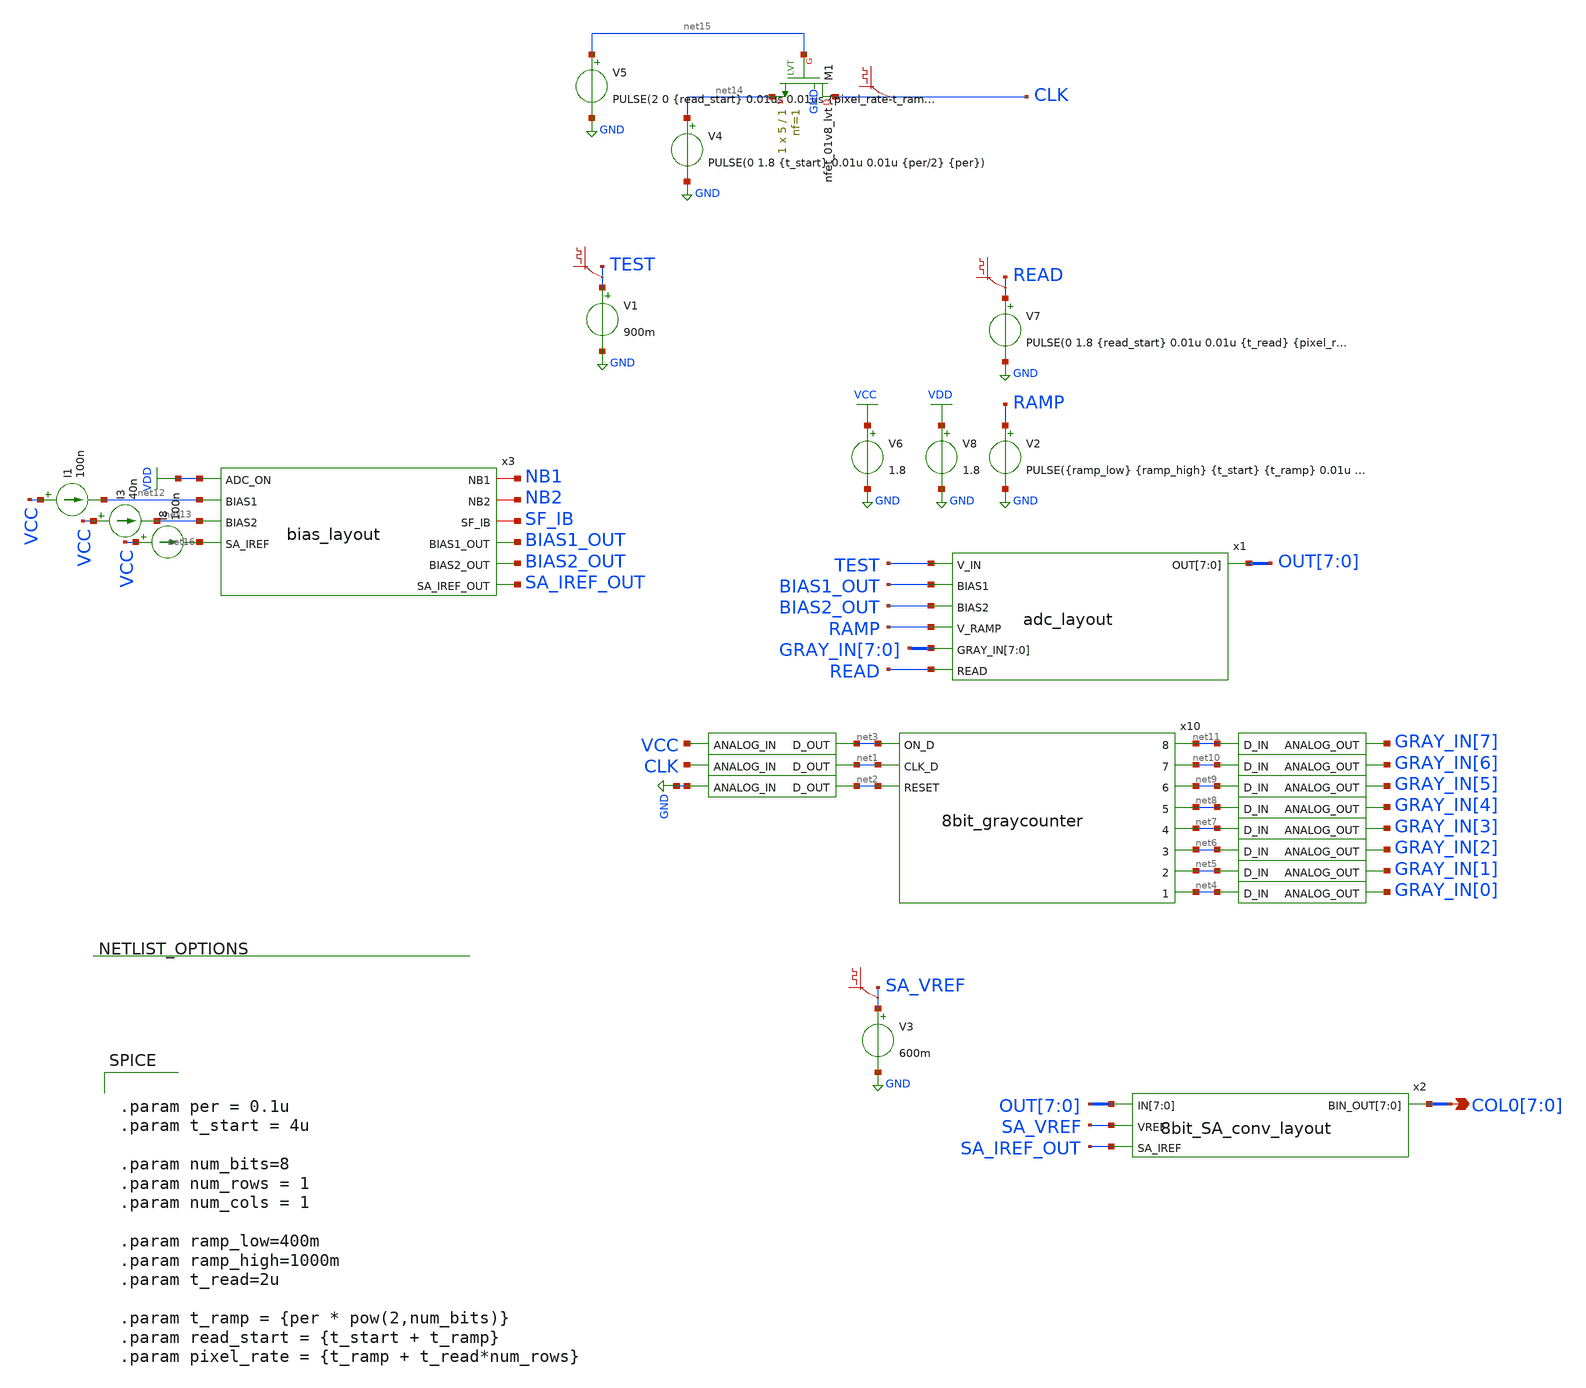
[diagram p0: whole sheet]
** sch_path: xschem/testbench/adc_layout_tb.sch
**.subckt adc_layout_tb COL0[7],COL0[6],COL0[5],COL0[4],COL0[3],COL0[2],COL0[1],COL0[0]
*.opin COL0[7],COL0[6],COL0[5],COL0[4],COL0[3],COL0[2],COL0[1],COL0[0]
V8 VDD GND 1.8
x6 net2 GND adc_bridge
x8 net3 VCC adc_bridge
x7 net1 CLK adc_bridge
x10 net11 net3 net10 net1 net9 net8 net2 net7 net6 net5 net4 8bit_graycounter
x5 GRAY_IN[7] net11 dac_bridge
x9 GRAY_IN[6] net10 dac_bridge
x11 GRAY_IN[5] net9 dac_bridge
x12 GRAY_IN[4] net8 dac_bridge
x13 GRAY_IN[3] net7 dac_bridge
x14 GRAY_IN[2] net6 dac_bridge
x15 GRAY_IN[1] net5 dac_bridge
x16 GRAY_IN[0] net4 dac_bridge
I1 VCC net12 100n
I3 VCC net13 40n
I8 VCC net16 100n
V2 RAMP GND PULSE({ramp_low} {ramp_high} {t_start} {t_ramp} 0.01u {pixel_rate-t_ramp} {pixel_rate})
V7 READ GND PULSE(0 1.8 {read_start} 0.01u 0.01u {t_read} {pixel_rate})
.save v(read)
V1 TEST GND 900m
.save v(test)
V3 SA_VREF GND 600m
.save v(sa_vref)
V4 net14 GND PULSE(0 1.8 {t_start} 0.01u 0.01u {per/2} {per})
V5 net15 GND PULSE(2 0 {read_start} 0.01us 0.01us {pixel_rate-t_ramp} {pixel_rate})
.save v(clk)
XM1 CLK net15 net14 GND sky130_fd_pr__nfet_01v8_lvt L=1 W=5 nf=1 ad='int((nf+1)/2) * W/nf * 0.29' as='int((nf+2)/2) * W/nf * 0.29'
+ pd='2*int((nf+1)/2) * (W/nf + 0.29)' ps='2*int((nf+2)/2) * (W/nf + 0.29)' nrd='0.29 / W' nrs='0.29 / W'
+ sa=0 sb=0 sd=0 mult=1 m=1
V6 VCC GND 1.8
x1 TEST BIAS1_OUT OUT[7] OUT[6] OUT[5] OUT[4] OUT[3] OUT[2] OUT[1] OUT[0] BIAS2_OUT RAMP GRAY_IN[7]
+ GRAY_IN[6] GRAY_IN[5] GRAY_IN[4] GRAY_IN[3] GRAY_IN[2] GRAY_IN[1] GRAY_IN[0] READ adc_layout
x2 OUT[7] OUT[6] OUT[5] OUT[4] OUT[3] OUT[2] OUT[1] OUT[0] SA_VREF SA_IREF_OUT COL0[7] COL0[6]
+ COL0[5] COL0[4] COL0[3] COL0[2] COL0[1] COL0[0] 8bit_SA_conv_layout
x3 NB1 NB2 SF_IB VDD net12 BIAS1_OUT BIAS2_OUT net13 SA_IREF_OUT net16 bias_layout
**** begin user architecture code


.param per = 0.1u
.param t_start = 4u

.param num_bits=8
.param num_rows = 1
.param num_cols = 1

.param ramp_low=400m
.param ramp_high=1000m
.param t_read=2u

.param t_ramp = {per * pow(2,num_bits)}
.param read_start = {t_start + t_ramp}
.param pixel_rate = {t_ramp + t_read*num_rows}



** opencircuitdesign pdks install
.lib $::SKYWATER_MODELS/sky130.lib.spice tt
.global vcc
.global vdd
.global gnd

**** end user architecture code
**.ends

* expanding   symbol:  digital_prims/adc_bridge.sym # of pins=2
** sym_path: xschem/digital_prims/adc_bridge.sym
** sch_path: xschem/digital_prims/adc_bridge.sch
.subckt adc_bridge D_OUT ANALOG_IN
*.ipin ANALOG_IN
*.opin D_OUT
**** begin user architecture code


abridge [ANALOG_IN] [D_OUT] adc_buff
.model adc_buff adc_bridge(in_low=0.9 in_high =0.9)


**** end user architecture code
.ends


* expanding   symbol:  adc/8bit_graycounter.sym # of pins=11
** sym_path: xschem/adc/8bit_graycounter.sym
** sch_path: xschem/adc/8bit_graycounter.sch
.subckt 8bit_graycounter 8 ON_D 7 CLK_D 6 5 RESET 4 3 2 1
*.ipin ON_D
*.ipin CLK_D
*.ipin RESET
*.opin 7
*.opin 6
*.opin 5
*.opin 4
*.opin 3
*.opin 2
*.opin 1
*.opin 8
**** begin user architecture code


a1 [ON_D] CLK_D RESET [8 7 6 5 4 3 2 1] gc_sm
.model gc_sm d_state(state_file="/home/hni/topmetal_dps/xschem/adc/graycntr.in")


**** end user architecture code
.ends


* expanding   symbol:  digital_prims/dac_bridge.sym # of pins=2
** sym_path: xschem/digital_prims/dac_bridge.sym
** sch_path: xschem/digital_prims/dac_bridge.sch
.subckt dac_bridge ANALOG_OUT D_IN
*.ipin D_IN
*.opin ANALOG_OUT
**** begin user architecture code


abridge_d [D_IN] [ANALOG_OUT] dac_buff
.model dac_buff dac_bridge(out_high=1.8)


**** end user architecture code
.ends


* expanding   symbol:  post_layout/adc_layout.sym # of pins=7
** sym_path: xschem/post_layout/adc_layout.sym
** sch_path: xschem/post_layout/adc_layout.sch
.subckt adc_layout V_IN BIAS1 OUT[7] OUT[6] OUT[5] OUT[4] OUT[3] OUT[2] OUT[1] OUT[0] BIAS2 V_RAMP
+ GRAY_IN[7] GRAY_IN[6] GRAY_IN[5] GRAY_IN[4] GRAY_IN[3] GRAY_IN[2] GRAY_IN[1] GRAY_IN[0] READ
*.ipin V_IN
*.ipin BIAS1
*.ipin BIAS2
*.ipin V_RAMP
*.ipin GRAY_IN[7],GRAY_IN[6],GRAY_IN[5],GRAY_IN[4],GRAY_IN[3],GRAY_IN[2],GRAY_IN[1],GRAY_IN[0]
*.ipin READ
*.opin OUT[7],OUT[6],OUT[5],OUT[4],OUT[3],OUT[2],OUT[1],OUT[0]
**** begin user architecture code


X8bit_dram_0 READ GRAY_INx4x GRAY_INx2x OUTx6x GRAY_INx7x READ GRAY_INx0x OUTx4x OUTx2x  GRAY_INx5x
+ GRAY_INx3x OUTx7x OUTx0x GRAY_INx1x OUTx3x OUTx5x READ 8bit_dram_0/4bit_dram_1/dram_array_1/dram_cell_1/WWL
+  OUTx1x GRAY_INx6x GND x8bit_dram
X0 VDD a_1000_n1450# a_1000_n1450# VDD sky130_fd_pr__pfet_01v8_lvt ad=1.45e+12p pd=1.09e+07u
+ as=3.5e+11p ps=2.7e+06u w=1e+06u l=1e+06u
X1 8bit_dram_0/4bit_dram_1/dram_array_1/dram_cell_1/WWL a_1870_n1400# GND GND
+ sky130_fd_pr__nfet_01v8 ad=4e+11p pd=2.8e+06u as=2.5e+07p ps=5000u w=1e+06u l=150000u
X2 a_1720_n1450# V_RAMP a_1100_n1450# GND sky130_fd_pr__nfet_01v8_lvt ad=3.5e+11p pd=2.7e+06u
+ as=8.8e+11p ps=7.1e+06u w=1e+06u l=150000u
X3 a_1870_n1400# a_1720_n1450# VDD VDD sky130_fd_pr__pfet_01v8_lvt ad=3.5e+11p pd=2.7e+06u as=0p
+ ps=0u w=1e+06u l=450000u
X4 a_1100_n1450# V_IN a_1000_n1450# GND sky130_fd_pr__nfet_01v8_lvt ad=0p pd=0u as=3.5e+11p
+ ps=2.7e+06u w=1e+06u l=150000u
X5 8bit_dram_0/4bit_dram_1/dram_array_1/dram_cell_1/WWL a_1870_n1400# VDD VDD
+ sky130_fd_pr__pfet_01v8 ad=3.5e+11p pd=2.7e+06u as=0p ps=0u w=1e+06u l=200000u
X6 a_1100_n1450# BIAS1 GND GND sky130_fd_pr__nfet_01v8 ad=0p pd=0u as=0p ps=0u w=450000u l=1e+06u
X7 a_1870_n1400# BIAS2 GND GND sky130_fd_pr__nfet_01v8_lvt ad=3.5e+11p pd=2.7e+06u as=0p ps=0u
+ w=1e+06u l=1e+06u
X8 a_1720_n1450# a_1000_n1450# VDD VDD sky130_fd_pr__pfet_01v8_lvt ad=3.5e+11p pd=2.7e+06u as=0p
+ ps=0u w=1e+06u l=1e+06u

.subckt dram_cell storage WWL WBL RWL RBL VSUBS
X0 RWL storage RBL VSUBS sky130_fd_pr__nfet_01v8 ad=3e+11p pd=2.6e+06u as=3.5e+11p ps=2.7e+06u
+ w=1e+06u l=150000u
X1 storage WWL WBL VSUBS sky130_fd_pr__nfet_01v8 ad=3.5e+11p pd=2.7e+06u as=3e+11p ps=2.6e+06u
+ w=1e+06u l=150000u
.ends

.subckt dram_array dram_cell_1/WWL dram_cell_0/WBL dram_cell_1/RWL dram_cell_0/RBL  dram_cell_1/WBL
+ dram_cell_1/RBL VSUBS dram_cell_0/RWL
Xdram_cell_0 dram_cell_0/storage dram_cell_1/WWL dram_cell_0/WBL dram_cell_0/RWL dram_cell_0/RBL
+  VSUBS dram_cell
Xdram_cell_1 dram_cell_1/storage dram_cell_1/WWL dram_cell_1/WBL dram_cell_1/RWL dram_cell_1/RBL
+  VSUBS dram_cell
.ends

.subckt x4bit_dram dram_array_0/dram_cell_1/RBL dram_array_1/dram_cell_0/RWL
+ dram_array_1/dram_cell_1/WWL  dram_array_1/dram_cell_0/WBL dram_array_0/dram_cell_0/WBL dram_array_1/dram_cell_1/RWL
+  dram_array_1/dram_cell_0/RBL dram_array_1/dram_cell_1/WBL dram_array_0/dram_cell_0/RBL  dram_array_0/dram_cell_1/WBL
+ dram_array_1/dram_cell_1/RBL VSUBS
Xdram_array_0 dram_array_1/dram_cell_1/WWL dram_array_0/dram_cell_0/WBL dram_array_1/dram_cell_0/RWL
+  dram_array_0/dram_cell_0/RBL dram_array_0/dram_cell_1/WBL dram_array_0/dram_cell_1/RBL  VSUBS dram_array_1/dram_cell_0/RWL
+ dram_array
Xdram_array_1 dram_array_1/dram_cell_1/WWL dram_array_1/dram_cell_0/WBL dram_array_1/dram_cell_1/RWL
+  dram_array_1/dram_cell_0/RBL dram_array_1/dram_cell_1/WBL dram_array_1/dram_cell_1/RBL  VSUBS dram_array_1/dram_cell_0/RWL
+ dram_array
.ends

.subckt x8bit_dram 4bit_dram_1/dram_array_1/dram_cell_1/RWL 4bit_dram_1/dram_array_0/dram_cell_0/WBL
+  4bit_dram_0/dram_array_1/dram_cell_0/WBL 4bit_dram_1/dram_array_1/dram_cell_0/RBL  4bit_dram_1/dram_array_1/dram_cell_1/WBL
+ 4bit_dram_0/dram_array_1/dram_cell_1/RWL  4bit_dram_0/dram_array_0/dram_cell_0/WBL 4bit_dram_1/dram_array_0/dram_cell_0/RBL
+  4bit_dram_0/dram_array_1/dram_cell_0/RBL 4bit_dram_1/dram_array_0/dram_cell_1/WBL  4bit_dram_0/dram_array_1/dram_cell_1/WBL
+ 4bit_dram_1/dram_array_1/dram_cell_1/RBL  4bit_dram_0/dram_array_0/dram_cell_0/RBL 4bit_dram_0/dram_array_0/dram_cell_1/WBL
+  4bit_dram_0/dram_array_1/dram_cell_1/RBL 4bit_dram_1/dram_array_0/dram_cell_1/RBL  4bit_dram_1/dram_array_1/dram_cell_0/RWL
+ 4bit_dram_1/dram_array_1/dram_cell_1/WWL  4bit_dram_0/dram_array_0/dram_cell_1/RBL 4bit_dram_1/dram_array_1/dram_cell_0/WBL  VSUBS
X4bit_dram_1 4bit_dram_1/dram_array_0/dram_cell_1/RBL 4bit_dram_1/dram_array_1/dram_cell_0/RWL
+  4bit_dram_1/dram_array_1/dram_cell_1/WWL 4bit_dram_1/dram_array_1/dram_cell_0/WBL  4bit_dram_1/dram_array_0/dram_cell_0/WBL
+ 4bit_dram_1/dram_array_1/dram_cell_1/RWL  4bit_dram_1/dram_array_1/dram_cell_0/RBL 4bit_dram_1/dram_array_1/dram_cell_1/WBL
+  4bit_dram_1/dram_array_0/dram_cell_0/RBL 4bit_dram_1/dram_array_0/dram_cell_1/WBL  4bit_dram_1/dram_array_1/dram_cell_1/RBL VSUBS x4bit_dram
X4bit_dram_0 4bit_dram_0/dram_array_0/dram_cell_1/RBL 4bit_dram_1/dram_array_1/dram_cell_0/RWL
+  4bit_dram_1/dram_array_1/dram_cell_1/WWL 4bit_dram_0/dram_array_1/dram_cell_0/WBL  4bit_dram_0/dram_array_0/dram_cell_0/WBL
+ 4bit_dram_0/dram_array_1/dram_cell_1/RWL  4bit_dram_0/dram_array_1/dram_cell_0/RBL 4bit_dram_0/dram_array_1/dram_cell_1/WBL
+  4bit_dram_0/dram_array_0/dram_cell_0/RBL 4bit_dram_0/dram_array_0/dram_cell_1/WBL  4bit_dram_0/dram_array_1/dram_cell_1/RBL VSUBS x4bit_dram
.ends




**** end user architecture code
.ends


* expanding   symbol:  post_layout/8bit_SA_conv_layout.sym # of pins=4
** sym_path: xschem/post_layout/8bit_SA_conv_layout.sym
** sch_path: xschem/post_layout/8bit_SA_conv_layout.sch
.subckt 8bit_SA_conv_layout IN[7] IN[6] IN[5] IN[4] IN[3] IN[2] IN[1] IN[0] VREF SA_IREF BIN_OUT[7]
+ BIN_OUT[6] BIN_OUT[5] BIN_OUT[4] BIN_OUT[3] BIN_OUT[2] BIN_OUT[1] BIN_OUT[0]
*.ipin IN[7],IN[6],IN[5],IN[4],IN[3],IN[2],IN[1],IN[0]
*.ipin VREF
*.opin BIN_OUT[7],BIN_OUT[6],BIN_OUT[5],BIN_OUT[4],BIN_OUT[3],BIN_OUT[2],BIN_OUT[1],BIN_OUT[0]
*.ipin SA_IREF
x11 net8 net9 net10 net7 net6 net11 net5 net12 net13 net4 net3 net14 net15 net2 net16 net1
+ 8bitgray2bin
x12 BIN_OUT[7] net8 dac_bridge
x13 BIN_OUT[6] net7 dac_bridge
x14 BIN_OUT[5] net6 dac_bridge
x16 BIN_OUT[4] net5 dac_bridge
x17 BIN_OUT[3] net4 dac_bridge
x18 BIN_OUT[2] net3 dac_bridge
x19 BIN_OUT[1] net2 dac_bridge
x37 BIN_OUT[0] net1 dac_bridge
x39 net9 OUT_A[7] adc_bridge
x40 net10 OUT_A[6] adc_bridge
x41 net11 OUT_A[5] adc_bridge
x42 net12 OUT_A[4] adc_bridge
x43 net13 OUT_A[3] adc_bridge
x44 net14 OUT_A[2] adc_bridge
x45 net15 OUT_A[1] adc_bridge
x46 net16 OUT_A[0] adc_bridge
.save v(bin_out[7])
.save v(bin_out[6])
.save v(bin_out[5])
.save v(bin_out[4])
.save v(bin_out[3])
.save v(bin_out[2])
.save v(bin_out[1])
.save v(bin_out[0])
**** begin user architecture code


Xsens_amp_2 INx5x SA_IREF OUT_Ax5x VREF VDD GND sens_amp
Xsens_amp_3 INx4x SA_IREF OUT_Ax4x VREF VDD GND sens_amp
Xsens_amp_4 INx3x SA_IREF OUT_Ax3x VREF VDD GND sens_amp
Xsens_amp_5 INx2x SA_IREF OUT_Ax2x VREF VDD GND sens_amp
Xsens_amp_6 INx1x SA_IREF OUT_Ax1x VREF VDD GND sens_amp
Xsens_amp_7 INx0x SA_IREF OUT_Ax0x VREF VDD GND sens_amp
Xsens_amp_0 INx7x SA_IREF OUT_Ax7x VREF VDD GND sens_amp
Xsens_amp_1 INx6x SA_IREF OUT_Ax6x VREF VDD GND sens_amp


.subckt sens_amp V_IN SA_IREF OUT REF VDD GND
X0 GN GN VDD VDD sky130_fd_pr__pfet_01v8_lvt ad=3.5e+11p pd=2.7e+06u as=1.8e+12p ps=1.22e+07u
+ w=1e+06u l=500000u
X1 net1 V_IN net2 GND sky130_fd_pr__nfet_01v8_lvt ad=1.4e+12p pd=8.7e+06u as=1.775e+12p ps=1.05e+07u
+ w=4e+06u l=150000u
X2 net2 REF GN GND sky130_fd_pr__nfet_01v8_lvt ad=0p pd=0u as=1.45e+12p ps=9.1e+06u w=4e+06u
+ l=150000u
X3 net1 GN VDD VDD sky130_fd_pr__pfet_01v8_lvt ad=3.5e+11p pd=2.7e+06u as=0p ps=0u w=1e+06u
+ l=500000u
X4 net2 SA_IREF GND GND sky130_fd_pr__nfet_01v8_lvt ad=0p pd=0u as=6e+11p ps=4.7e+06u w=500000u
+ l=1e+06u
X5 OUT net1 VDD VDD sky130_fd_pr__pfet_01v8_lvt ad=1.05e+12p pd=6.7e+06u as=0p ps=0u w=3e+06u
+ l=350000u
X6 OUT net1 GND GND sky130_fd_pr__nfet_01v8_lvt ad=3.5e+11p pd=2.7e+06u as=0p ps=0u w=1e+06u
+ l=150000u
.ends




**** end user architecture code
.ends


* expanding   symbol:  post_layout/bias_layout.sym # of pins=10
** sym_path: xschem/post_layout/bias_layout.sym
** sch_path: xschem/post_layout/bias_layout.sch
.subckt bias_layout NB1 NB2 SF_IB ADC_ON BIAS1 BIAS1_OUT BIAS2_OUT BIAS2 SA_IREF_OUT SA_IREF
*.iopin SF_IB
*.iopin NB2
*.ipin ADC_ON
*.ipin BIAS1
*.opin BIAS1_OUT
*.ipin BIAS2
*.opin BIAS2_OUT
*.ipin SA_IREF
*.opin SA_IREF_OUT
*.iopin NB1
**** begin user architecture code


X0 BIAS1 ADC_ON BIAS1_OUT GND sky130_fd_pr__nfet_01v8 ad=2.5e+12p pd=1.1e+07u as=5.9425e+12p
+ ps=1.514e+07u w=5e+06u l=1e+06u
X1 NB1 NB1 GND GND sky130_fd_pr__nfet_01v8_lvt ad=3.5e+11p pd=2.7e+06u as=1.272e+13p ps=4.894e+07u
+ w=1e+06u l=1.2e+06u
X2 BIAS2_OUT BIAS2_OUT GND GND sky130_fd_pr__nfet_01v8_lvt ad=5.9725e+12p pd=1.52e+07u as=0p ps=0u
+ w=1e+06u l=1e+06u
X3 SA_IREF_OUT SA_IREF_OUT GND GND sky130_fd_pr__nfet_01v8 ad=5.9905e+12p pd=1.53e+07u as=0p ps=0u
+ w=500000u l=1e+06u
X4 NB2 NB2 GND GND sky130_fd_pr__nfet_01v8_lvt ad=3.5e+11p pd=2.7e+06u as=0p ps=0u w=1e+06u
+ l=1.2e+06u
X5 BIAS2 ADC_ON BIAS2_OUT GND sky130_fd_pr__nfet_01v8 ad=2.5e+12p pd=1.1e+07u as=0p ps=0u w=5e+06u
+ l=1e+06u
X6 AMP_IB AMP_IB GND GND sky130_fd_pr__nfet_01v8_lvt ad=5.6e+12p pd=1.74e+07u as=0p ps=0u w=8e+06u
+ l=2e+06u
X7 OUT_IB OUT_IB GND GND sky130_fd_pr__nfet_01v8_lvt ad=5.6e+12p pd=1.74e+07u as=0p ps=0u w=8e+06u
+ l=2e+06u
X8 SA_IREF ADC_ON SA_IREF_OUT GND sky130_fd_pr__nfet_01v8 ad=2.5e+12p pd=1.1e+07u as=0p ps=0u
+ w=5e+06u l=1e+06u
X9 BIAS1_OUT BIAS1_OUT GND GND sky130_fd_pr__nfet_01v8 ad=0p pd=0u as=0p ps=0u w=420000u l=1e+06u
X10 SF_IB SF_IB VDD VDD sky130_fd_pr__pfet_01v8_lvt ad=5.5e+11p pd=3.1e+06u as=4.5e+11p ps=2.9e+06u
+ w=1e+06u l=1e+06u




**** end user architecture code
.ends


* expanding   symbol:  adc/8bitgray2bin.sym # of pins=16
** sym_path: xschem/adc/8bitgray2bin.sym
** sch_path: xschem/adc/8bitgray2bin.sch
.subckt 8bitgray2bin 8 g8 g7 7 6 g6 5 g5 g4 4 3 g3 g2 2 g1 1
*.opin 7
*.opin 6
*.opin 5
*.opin 4
*.opin 3
*.opin 2
*.opin 1
*.opin 8
*.ipin g5
*.ipin g4
*.ipin g3
*.ipin g8
*.ipin g7
*.ipin g6
*.ipin g2
*.ipin g1
**** begin user architecture code


* lsb first.
a1 [g1 g2 g3 g4 g5 g6 g7 g8] [1 2 3 4 5 6 7 8] gray2bin_lut
.model gray2bin_lut d_genlut(rise_delay=[1p 1p] fall_delay=[1p 1p]  input_load=[1p 1p]
+ input_delay=[0 0]
+ table_values=01101001100101101001011001101001100101100110100101101001100101101001011001101001011010011001011001101001100101101001011001101001100101100110100101101001100101100110100110010110100101100110100101101001100101101001011001101001100101100110100101101001100101100011110011000011110000110011110011000011001111000011110011000011110000110011110000111100110000110011110011000011110000110011110011000011001111000011110011000011001111001100001111000011001111000011110011000011110000110011110011000011001111000011110011000011000011111111000011110000000011111111000000001111000011111111000011110000000011110000111111110000000011111111000011110000000011111111000000001111000011111111000000001111111100001111000000001111000011111111000011110000000011111111000000001111000011111111000000000000111111111111111100000000111111110000000000000000111111111111111100000000000000001111111100000000111111111111111100000000111111110000000000000000111111110000000011111111111111110000000000000000111111111111111100000000111111110000000000000000111111110000000000000000111111111111111111111111111111110000000000000000111111111111111100000000000000000000000000000000111111111111111111111111111111110000000000000000000000000000000011111111111111110000000000000000111111111111111111111111111111110000000000000000000000000000000000000000000000001111111111111111111111111111111111111111111111111111111111111111000000000000000000000000000000001111111111111111111111111111111100000000000000000000000000000000000000000000000000000000000000001111111111111111111111111111111100000000000000000000000000000000000000000000000000000000000000001111111111111111111111111111111111111111111111111111111111111111111111111111111111111111111111111111111111111111111111111111111100000000000000000000000000000000000000000000000000000000000000000000000000000000000000000000000000000000000000000000000000000000000000000000000000000000000000000000000000000000000000000000000011111111111111111111111111111111111111111111111111111111111111111111111111111111111111111111111111111111111111111111111111111111)




**** end user architecture code
.ends

.GLOBAL GND
.GLOBAL VDD
.GLOBAL VCC
**** begin user architecture code


.options gmin=10e-20
.control
save all

*dc v2 0 1.8 0.05
*plot v(test)
tran 1u 200u

write adc_layout_tb.raw
.endc


**** end user architecture code
.end
